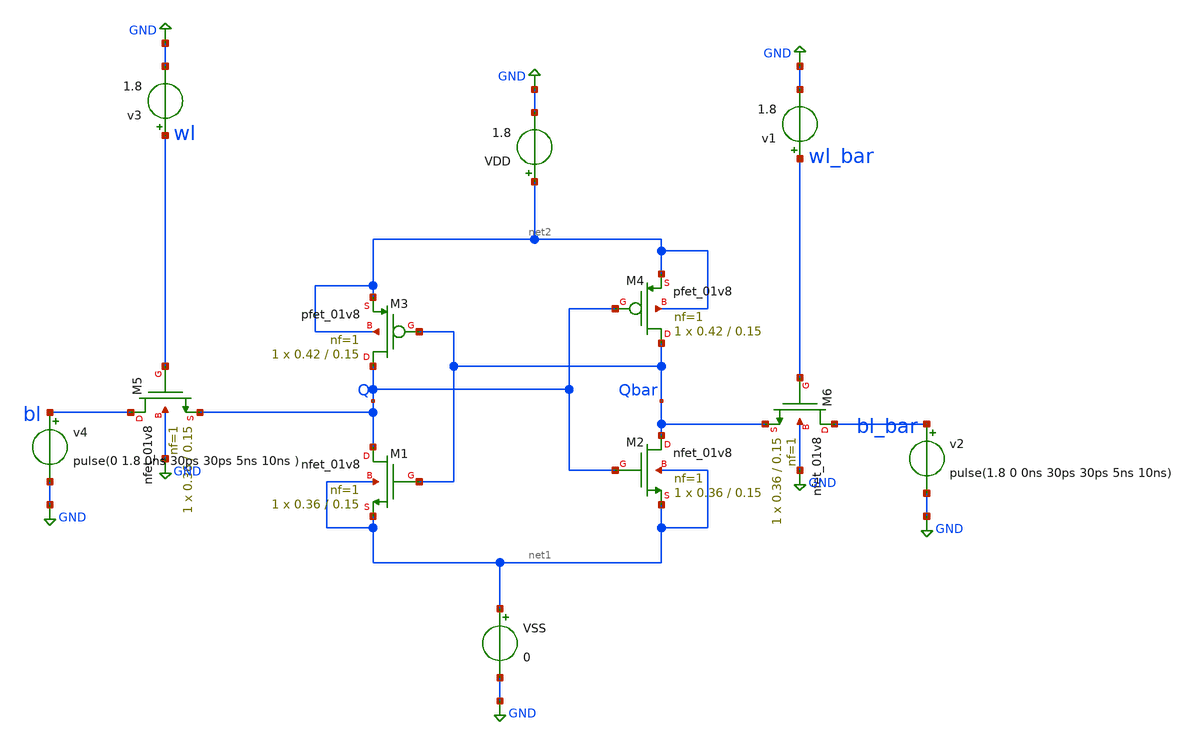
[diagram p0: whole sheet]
** sch_path: nikhil/SRAM/6T_PIM_TEST.sch
**.subckt 6T_PIM_TEST
VDD net2 GND 1.8
v3 wl GND 1.8
v2 bl_bar GND pulse(1.8 0 0ns 30ps 30ps 5ns 10ns)
XM2 Qbar Q net1 net1 sky130_fd_pr__nfet_01v8 L=0.15 W=0.36 nf=1 ad='int((nf+1)/2) * W/nf * 0.29' as='int((nf+2)/2) * W/nf * 0.29'
+ pd='2*int((nf+1)/2) * (W/nf + 0.29)' ps='2*int((nf+2)/2) * (W/nf + 0.29)' nrd='0.29 / W' nrs='0.29 / W'
+ sa=0 sb=0 sd=0 mult=1 m=1
XM3 Q Qbar net2 net2 sky130_fd_pr__pfet_01v8 L=0.15 W=0.42 nf=1 ad='int((nf+1)/2) * W/nf * 0.29' as='int((nf+2)/2) * W/nf * 0.29'
+ pd='2*int((nf+1)/2) * (W/nf + 0.29)' ps='2*int((nf+2)/2) * (W/nf + 0.29)' nrd='0.29 / W' nrs='0.29 / W'
+ sa=0 sb=0 sd=0 mult=1 m=1
XM4 Qbar Q net2 net2 sky130_fd_pr__pfet_01v8 L=0.15 W=0.42 nf=1 ad='int((nf+1)/2) * W/nf * 0.29' as='int((nf+2)/2) * W/nf * 0.29'
+ pd='2*int((nf+1)/2) * (W/nf + 0.29)' ps='2*int((nf+2)/2) * (W/nf + 0.29)' nrd='0.29 / W' nrs='0.29 / W'
+ sa=0 sb=0 sd=0 mult=1 m=1
XM5 bl wl Q GND sky130_fd_pr__nfet_01v8 L=0.15 W=0.36 nf=1 ad='int((nf+1)/2) * W/nf * 0.29' as='int((nf+2)/2) * W/nf * 0.29'
+ pd='2*int((nf+1)/2) * (W/nf + 0.29)' ps='2*int((nf+2)/2) * (W/nf + 0.29)' nrd='0.29 / W' nrs='0.29 / W'
+ sa=0 sb=0 sd=0 mult=1 m=1
XM6 bl_bar wl_bar Qbar GND sky130_fd_pr__nfet_01v8 L=0.15 W=0.36 nf=1 ad='int((nf+1)/2) * W/nf * 0.29'
+ as='int((nf+2)/2) * W/nf * 0.29' pd='2*int((nf+1)/2) * (W/nf + 0.29)' ps='2*int((nf+2)/2) * (W/nf + 0.29)'
+ nrd='0.29 / W' nrs='0.29 / W' sa=0 sb=0 sd=0 mult=1 m=1
XM1 Q Qbar net1 net1 sky130_fd_pr__nfet_01v8 L=0.15 W=0.36 nf=1 ad='int((nf+1)/2) * W/nf * 0.29' as='int((nf+2)/2) * W/nf * 0.29'
+ pd='2*int((nf+1)/2) * (W/nf + 0.29)' ps='2*int((nf+2)/2) * (W/nf + 0.29)' nrd='0.29 / W' nrs='0.29 / W'
+ sa=0 sb=0 sd=0 mult=1 m=1
VSS net1 GND 0
v4 bl GND pulse(0 1.8 0ns 30ps 30ps 5ns 10ns )
v1 wl_bar GND 1.8
**** begin user architecture code

.tran


.options wnflag=1
.include /pdk/open_pdks/sources/sky130-pdk/libraries/sky130_fd_pr/latest/cells/nfet_01v8/sky130_fd_pr__nfet_01v8__tt.corner.spice
.include /pdk/open_pdks/sources/sky130-pdk/libraries/sky130_fd_pr/latest/cells/nfet_01v8_lvt/sky130_fd_pr__nfet_01v8_lvt__tt.corner.spice
.include /pdk/open_pdks/sources/sky130-pdk/libraries/sky130_fd_pr/latest/cells/pfet_01v8/sky130_fd_pr__pfet_01v8__tt.corner.spice
.include /pdk/open_pdks/sources/sky130-pdk/libraries/sky130_fd_pr/latest/cells/nfet_03v3_nvt/sky130_fd_pr__nfet_03v3_nvt__tt.corner.spice
.include /pdk/open_pdks/sources/sky130-pdk/libraries/sky130_fd_pr/latest/cells/nfet_05v0_nvt/sky130_fd_pr__nfet_05v0_nvt__tt.corner.spice
.include /pdk/open_pdks/sources/sky130-pdk/libraries/sky130_fd_pr/latest/cells/esd_nfet_01v8/sky130_fd_pr__esd_nfet_01v8__tt.corner.spice
.include /pdk/open_pdks/sources/sky130-pdk/libraries/sky130_fd_pr/latest/cells/pfet_01v8_lvt/sky130_fd_pr__pfet_01v8_lvt__tt.corner.spice
.include /pdk/open_pdks/sources/sky130-pdk/libraries/sky130_fd_pr/latest/cells/pfet_01v8_hvt/sky130_fd_pr__pfet_01v8_hvt__tt.corner.spice
.include /pdk/open_pdks/sources/sky130-pdk/libraries/sky130_fd_pr/latest/cells/esd_pfet_g5v0d10v5/sky130_fd_pr__esd_pfet_g5v0d10v5__tt.corner.spice
.include /pdk/open_pdks/sources/sky130-pdk/libraries/sky130_fd_pr/latest/cells/pfet_g5v0d10v5/sky130_fd_pr__pfet_g5v0d10v5__tt.corner.spice
.include /pdk/open_pdks/sources/sky130-pdk/libraries/sky130_fd_pr/latest/cells/pfet_g5v0d16v0/sky130_fd_pr__pfet_g5v0d16v0__tt.corner.spice
.include /pdk/open_pdks/sources/sky130-pdk/libraries/sky130_fd_pr/latest/cells/nfet_g5v0d10v5/sky130_fd_pr__nfet_g5v0d10v5__tt.corner.spice
.include /pdk/open_pdks/sources/sky130-pdk/libraries/sky130_fd_pr/latest/cells/nfet_g5v0d16v0/sky130_fd_pr__nfet_g5v0d16v0__tt_discrete.corner.spice
.include /pdk/open_pdks/sources/sky130-pdk/libraries/sky130_fd_pr/latest/cells/esd_nfet_g5v0d10v5/sky130_fd_pr__esd_nfet_g5v0d10v5__tt.corner.spice
.include /pdk/open_pdks/sources/sky130-pdk/libraries/sky130_fd_pr/latest/models/corners/tt/nonfet.spice
* Mismatch parameters
.include /pdk/open_pdks/sources/sky130-pdk/libraries/sky130_fd_pr/latest/cells/nfet_01v8/sky130_fd_pr__nfet_01v8__mismatch.corner.spice
.include /pdk/open_pdks/sources/sky130-pdk/libraries/sky130_fd_pr/latest/cells/pfet_01v8/sky130_fd_pr__pfet_01v8__mismatch.corner.spice
.include /pdk/open_pdks/sources/sky130-pdk/libraries/sky130_fd_pr/latest/cells/nfet_01v8_lvt/sky130_fd_pr__nfet_01v8_lvt__mismatch.corner.spice
.include /pdk/open_pdks/sources/sky130-pdk/libraries/sky130_fd_pr/latest/cells/pfet_01v8_lvt/sky130_fd_pr__pfet_01v8_lvt__mismatch.corner.spice
.include /pdk/open_pdks/sources/sky130-pdk/libraries/sky130_fd_pr/latest/cells/pfet_01v8_hvt/sky130_fd_pr__pfet_01v8_hvt__mismatch.corner.spice
.include /pdk/open_pdks/sources/sky130-pdk/libraries/sky130_fd_pr/latest/cells/nfet_g5v0d10v5/sky130_fd_pr__nfet_g5v0d10v5__mismatch.corner.spice
.include /pdk/open_pdks/sources/sky130-pdk/libraries/sky130_fd_pr/latest/cells/pfet_g5v0d10v5/sky130_fd_pr__pfet_g5v0d10v5__mismatch.corner.spice
.include /pdk/open_pdks/sources/sky130-pdk/libraries/sky130_fd_pr/latest/cells/nfet_05v0_nvt/sky130_fd_pr__nfet_05v0_nvt__mismatch.corner.spice
.include /pdk/open_pdks/sources/sky130-pdk/libraries/sky130_fd_pr/latest/cells/nfet_03v3_nvt/sky130_fd_pr__nfet_03v3_nvt__mismatch.corner.spice
* Resistor$::SKYWATER_MODELS/Capacitor
.include /pdk/open_pdks/sources/sky130-pdk/libraries/sky130_fd_pr/latest/models/r+c/res_typical__cap_typical.spice
.include /pdk/open_pdks/sources/sky130-pdk/libraries/sky130_fd_pr/latest/models/r+c/res_typical__cap_typical__lin.spice
* Special cells
.include /pdk/open_pdks/sources/sky130-pdk/libraries/sky130_fd_pr/latest/models/corners/tt/specialized_cells.spice
* All models
.include /pdk/open_pdks/sources/sky130-pdk/libraries/sky130_fd_pr/latest/models/all.spice
* Corner
.include /pdk/open_pdks/sources/sky130-pdk/libraries/sky130_fd_pr/latest/models/corners/tt/rf.spice

**** end user architecture code
**.ends
.GLOBAL GND
.end
